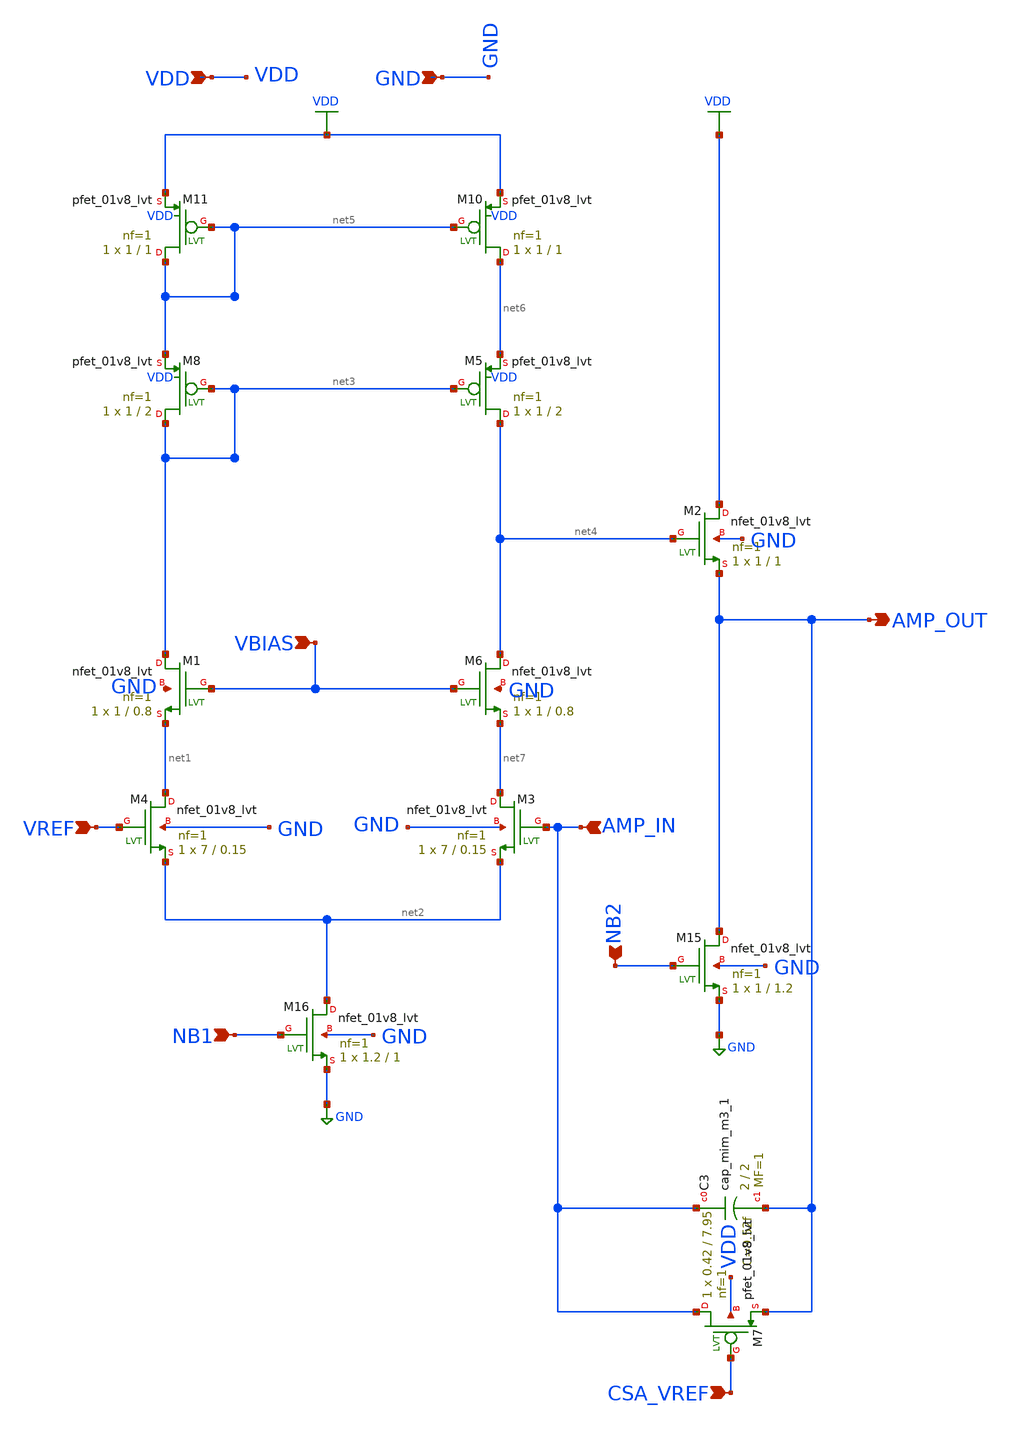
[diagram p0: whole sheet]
** sch_path: xschem/csa.sch
**.subckt csa VREF AMP_IN NB1 CSA_VREF VBIAS AMP_OUT NB2 VDD GND
*.ipin VREF
*.ipin AMP_IN
*.ipin NB1
*.ipin CSA_VREF
*.ipin VBIAS
*.opin AMP_OUT
*.ipin NB2
*.ipin VDD
*.ipin GND
XM2 VDD net4 AMP_OUT GND sky130_fd_pr__nfet_01v8_lvt L=1 W=1 nf=1 ad='int((nf+1)/2) * W/nf * 0.29' as='int((nf+2)/2) * W/nf * 0.29'
+ pd='2*int((nf+1)/2) * (W/nf + 0.29)' ps='2*int((nf+2)/2) * (W/nf + 0.29)' nrd='0.29 / W' nrs='0.29 / W'
+ sa=0 sb=0 sd=0 mult=1 m=1
XM8 net3 net3 net5 VDD sky130_fd_pr__pfet_01v8_lvt L=2 W=1 nf=1 ad='int((nf+1)/2) * W/nf * 0.29' as='int((nf+2)/2) * W/nf * 0.29'
+ pd='2*int((nf+1)/2) * (W/nf + 0.29)' ps='2*int((nf+2)/2) * (W/nf + 0.29)' nrd='0.29 / W' nrs='0.29 / W'
+ sa=0 sb=0 sd=0 mult=1 m=1
XM10 net6 net5 VDD VDD sky130_fd_pr__pfet_01v8_lvt L=1 W=1 nf=1 ad='int((nf+1)/2) * W/nf * 0.29' as='int((nf+2)/2) * W/nf * 0.29'
+ pd='2*int((nf+1)/2) * (W/nf + 0.29)' ps='2*int((nf+2)/2) * (W/nf + 0.29)' nrd='0.29 / W' nrs='0.29 / W'
+ sa=0 sb=0 sd=0 mult=1 m=1
XM11 net5 net5 VDD VDD sky130_fd_pr__pfet_01v8_lvt L=1 W=1 nf=1 ad='int((nf+1)/2) * W/nf * 0.29' as='int((nf+2)/2) * W/nf * 0.29'
+ pd='2*int((nf+1)/2) * (W/nf + 0.29)' ps='2*int((nf+2)/2) * (W/nf + 0.29)' nrd='0.29 / W' nrs='0.29 / W'
+ sa=0 sb=0 sd=0 mult=1 m=1
XM15 AMP_OUT NB2 GND GND sky130_fd_pr__nfet_01v8_lvt L=1.2 W=1 nf=1 ad='int((nf+1)/2) * W/nf * 0.29'
+ as='int((nf+2)/2) * W/nf * 0.29' pd='2*int((nf+1)/2) * (W/nf + 0.29)' ps='2*int((nf+2)/2) * (W/nf + 0.29)'
+ nrd='0.29 / W' nrs='0.29 / W' sa=0 sb=0 sd=0 mult=1 m=1
XM16 net2 NB1 GND GND sky130_fd_pr__nfet_01v8_lvt L=1 W=1.2 nf=1 ad='int((nf+1)/2) * W/nf * 0.29' as='int((nf+2)/2) * W/nf * 0.29'
+ pd='2*int((nf+1)/2) * (W/nf + 0.29)' ps='2*int((nf+2)/2) * (W/nf + 0.29)' nrd='0.29 / W' nrs='0.29 / W'
+ sa=0 sb=0 sd=0 mult=1 m=1
XC3 AMP_IN AMP_OUT sky130_fd_pr__cap_mim_m3_1 W=2 L=2 MF=1 m=1
XM4 net1 VREF net2 GND sky130_fd_pr__nfet_01v8_lvt L=0.15 W=7 nf=1 ad='int((nf+1)/2) * W/nf * 0.29' as='int((nf+2)/2) * W/nf * 0.29'
+ pd='2*int((nf+1)/2) * (W/nf + 0.29)' ps='2*int((nf+2)/2) * (W/nf + 0.29)' nrd='0.29 / W' nrs='0.29 / W'
+ sa=0 sb=0 sd=0 mult=1 m=1
XM7 AMP_IN CSA_VREF AMP_OUT VDD sky130_fd_pr__pfet_01v8_lvt L=7.95 W=0.42 nf=1 ad='int((nf+1)/2) * W/nf * 0.29'
+ as='int((nf+2)/2) * W/nf * 0.29' pd='2*int((nf+1)/2) * (W/nf + 0.29)' ps='2*int((nf+2)/2) * (W/nf + 0.29)'
+ nrd='0.29 / W' nrs='0.29 / W' sa=0 sb=0 sd=0 mult=1 m=1
XM5 net4 net3 net6 VDD sky130_fd_pr__pfet_01v8_lvt L=2 W=1 nf=1 ad='int((nf+1)/2) * W/nf * 0.29' as='int((nf+2)/2) * W/nf * 0.29'
+ pd='2*int((nf+1)/2) * (W/nf + 0.29)' ps='2*int((nf+2)/2) * (W/nf + 0.29)' nrd='0.29 / W' nrs='0.29 / W'
+ sa=0 sb=0 sd=0 mult=1 m=1
XM1 net3 VBIAS net1 GND sky130_fd_pr__nfet_01v8_lvt L=0.8 W=1 nf=1 ad='int((nf+1)/2) * W/nf * 0.29' as='int((nf+2)/2) * W/nf * 0.29'
+ pd='2*int((nf+1)/2) * (W/nf + 0.29)' ps='2*int((nf+2)/2) * (W/nf + 0.29)' nrd='0.29 / W' nrs='0.29 / W'
+ sa=0 sb=0 sd=0 mult=1 m=1
XM3 net7 AMP_IN net2 GND sky130_fd_pr__nfet_01v8_lvt L=0.15 W=7 nf=1 ad='int((nf+1)/2) * W/nf * 0.29'
+ as='int((nf+2)/2) * W/nf * 0.29' pd='2*int((nf+1)/2) * (W/nf + 0.29)' ps='2*int((nf+2)/2) * (W/nf + 0.29)'
+ nrd='0.29 / W' nrs='0.29 / W' sa=0 sb=0 sd=0 mult=1 m=1
XM6 net4 VBIAS net7 GND sky130_fd_pr__nfet_01v8_lvt L=0.8 W=1 nf=1 ad='int((nf+1)/2) * W/nf * 0.29' as='int((nf+2)/2) * W/nf * 0.29'
+ pd='2*int((nf+1)/2) * (W/nf + 0.29)' ps='2*int((nf+2)/2) * (W/nf + 0.29)' nrd='0.29 / W' nrs='0.29 / W'
+ sa=0 sb=0 sd=0 mult=1 m=1
**.ends
.GLOBAL VDD
.GLOBAL GND
.end
